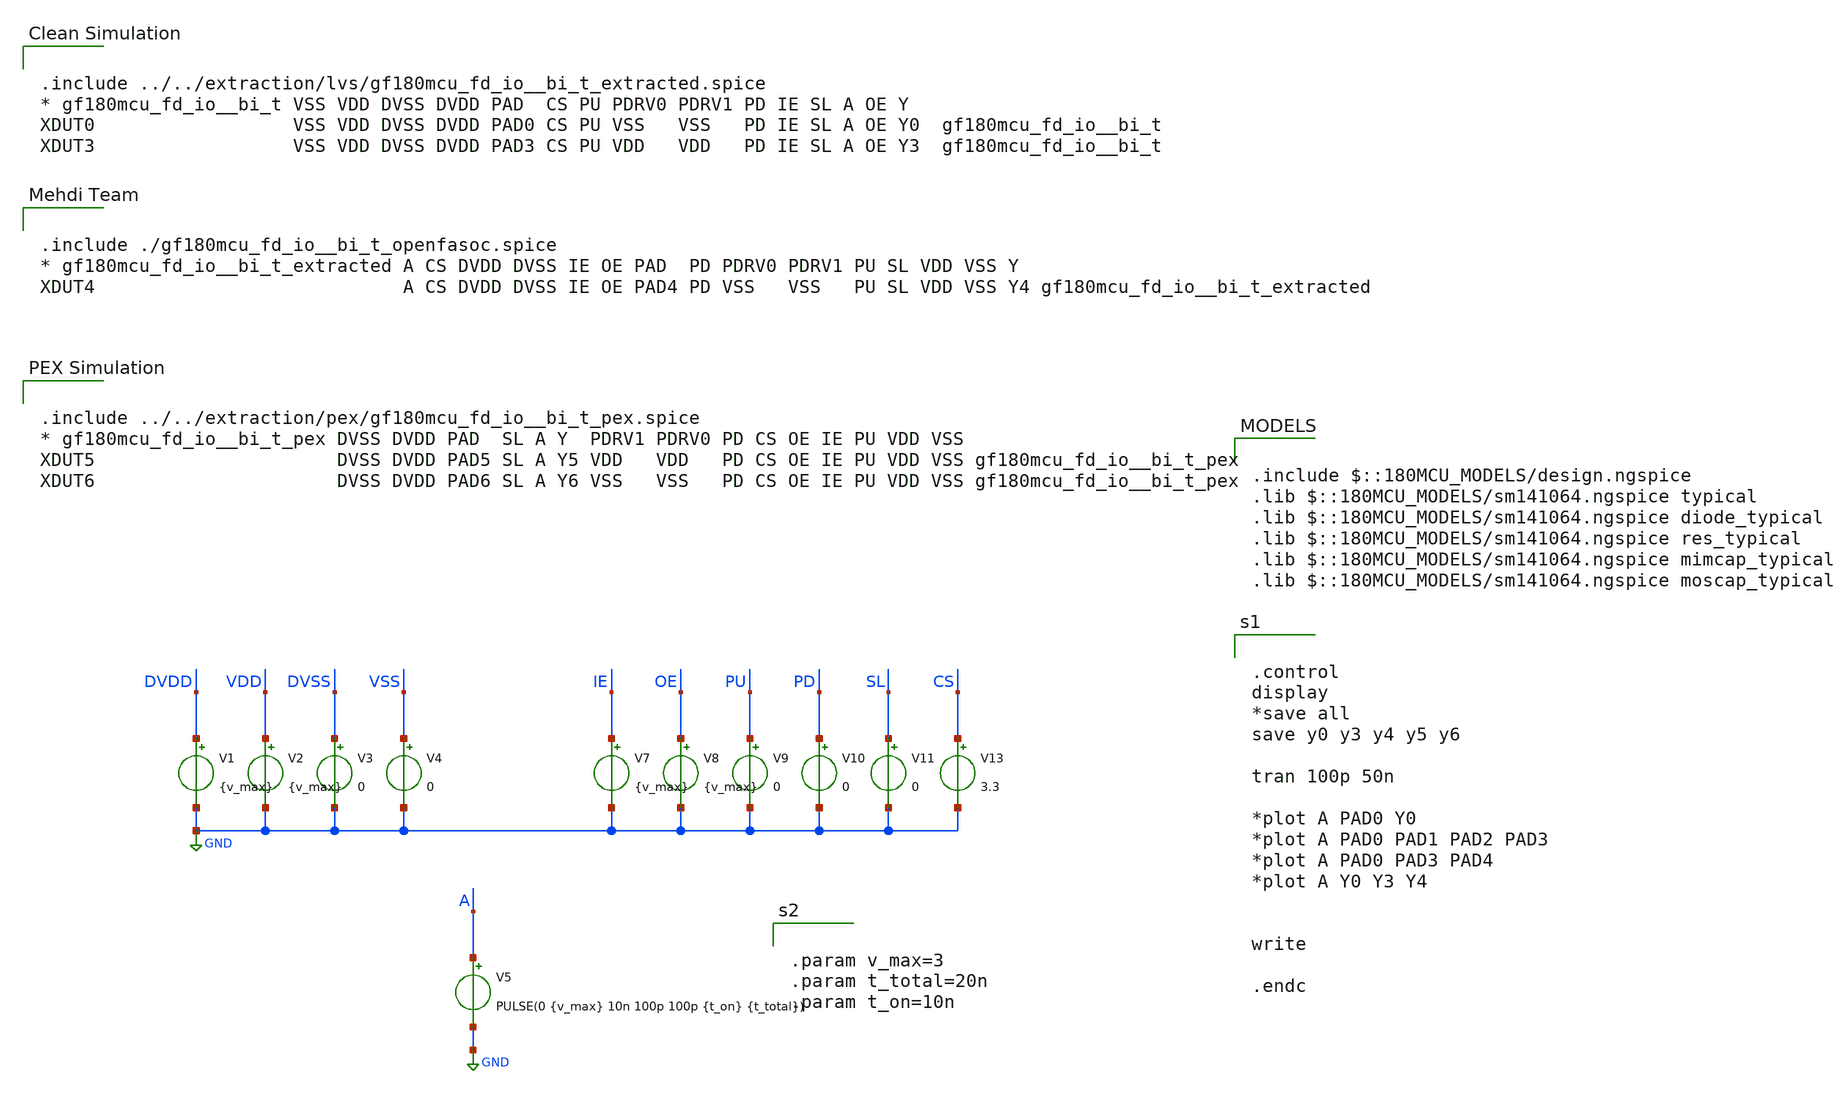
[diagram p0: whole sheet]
** sch_path: test/bi_t_switch/bi_t_switch.sch


.param v_max=3
.param t_total=20n
.param t_on=10n


**.subckt bi_t_switch
V1 DVDD GND {v_max}
V2 VDD GND {v_max}
V3 DVSS GND 0
V4 VSS GND 0
V5 A GND PULSE(0 {v_max} 10n 100p 100p {t_on} {t_total})
V7 IE GND {v_max}
V8 OE GND {v_max}
V9 PU GND 0
V10 PD GND 0
V11 SL GND 0
V13 CS GND 3.3
**** begin user architecture code


.control
display
*save all
save y0 y3 y4 y5 y6

tran 100p 50n

*plot A PAD0 Y0
*plot A PAD0 PAD1 PAD2 PAD3
*plot A PAD0 PAD3 PAD4
*plot A Y0 Y3 Y4


write

.endc



.include $::180MCU_MODELS/design.ngspice
.lib $::180MCU_MODELS/sm141064.ngspice typical
.lib $::180MCU_MODELS/sm141064.ngspice diode_typical
.lib $::180MCU_MODELS/sm141064.ngspice res_typical
.lib $::180MCU_MODELS/sm141064.ngspice mimcap_typical
.lib $::180MCU_MODELS/sm141064.ngspice moscap_typical


.include ./gf180mcu_fd_io__bi_t_openfasoc.spice
* gf180mcu_fd_io__bi_t_extracted A CS DVDD DVSS IE OE PAD  PD PDRV0 PDRV1 PU SL VDD VSS Y
XDUT4                            A CS DVDD DVSS IE OE PAD4 PD VSS   VSS   PU SL VDD VSS Y4
+ gf180mcu_fd_io__bi_t_extracted


.include ../../extraction/pex/gf180mcu_fd_io__bi_t_pex.spice
* gf180mcu_fd_io__bi_t_pex DVSS DVDD PAD  SL A Y  PDRV1 PDRV0 PD CS OE IE PU VDD VSS
XDUT5                      DVSS DVDD PAD5 SL A Y5 VDD   VDD   PD CS OE IE PU VDD VSS
+ gf180mcu_fd_io__bi_t_pex
XDUT6                      DVSS DVDD PAD6 SL A Y6 VSS   VSS   PD CS OE IE PU VDD VSS
+ gf180mcu_fd_io__bi_t_pex


.include ../../extraction/lvs/gf180mcu_fd_io__bi_t_extracted.spice
* gf180mcu_fd_io__bi_t VSS VDD DVSS DVDD PAD  CS PU PDRV0 PDRV1 PD IE SL A OE Y
XDUT0                  VSS VDD DVSS DVDD PAD0 CS PU VSS   VSS   PD IE SL A OE Y0
+  gf180mcu_fd_io__bi_t
XDUT3                  VSS VDD DVSS DVDD PAD3 CS PU VDD   VDD   PD IE SL A OE Y3
+  gf180mcu_fd_io__bi_t

**** end user architecture code
**.ends
.GLOBAL GND
.end
